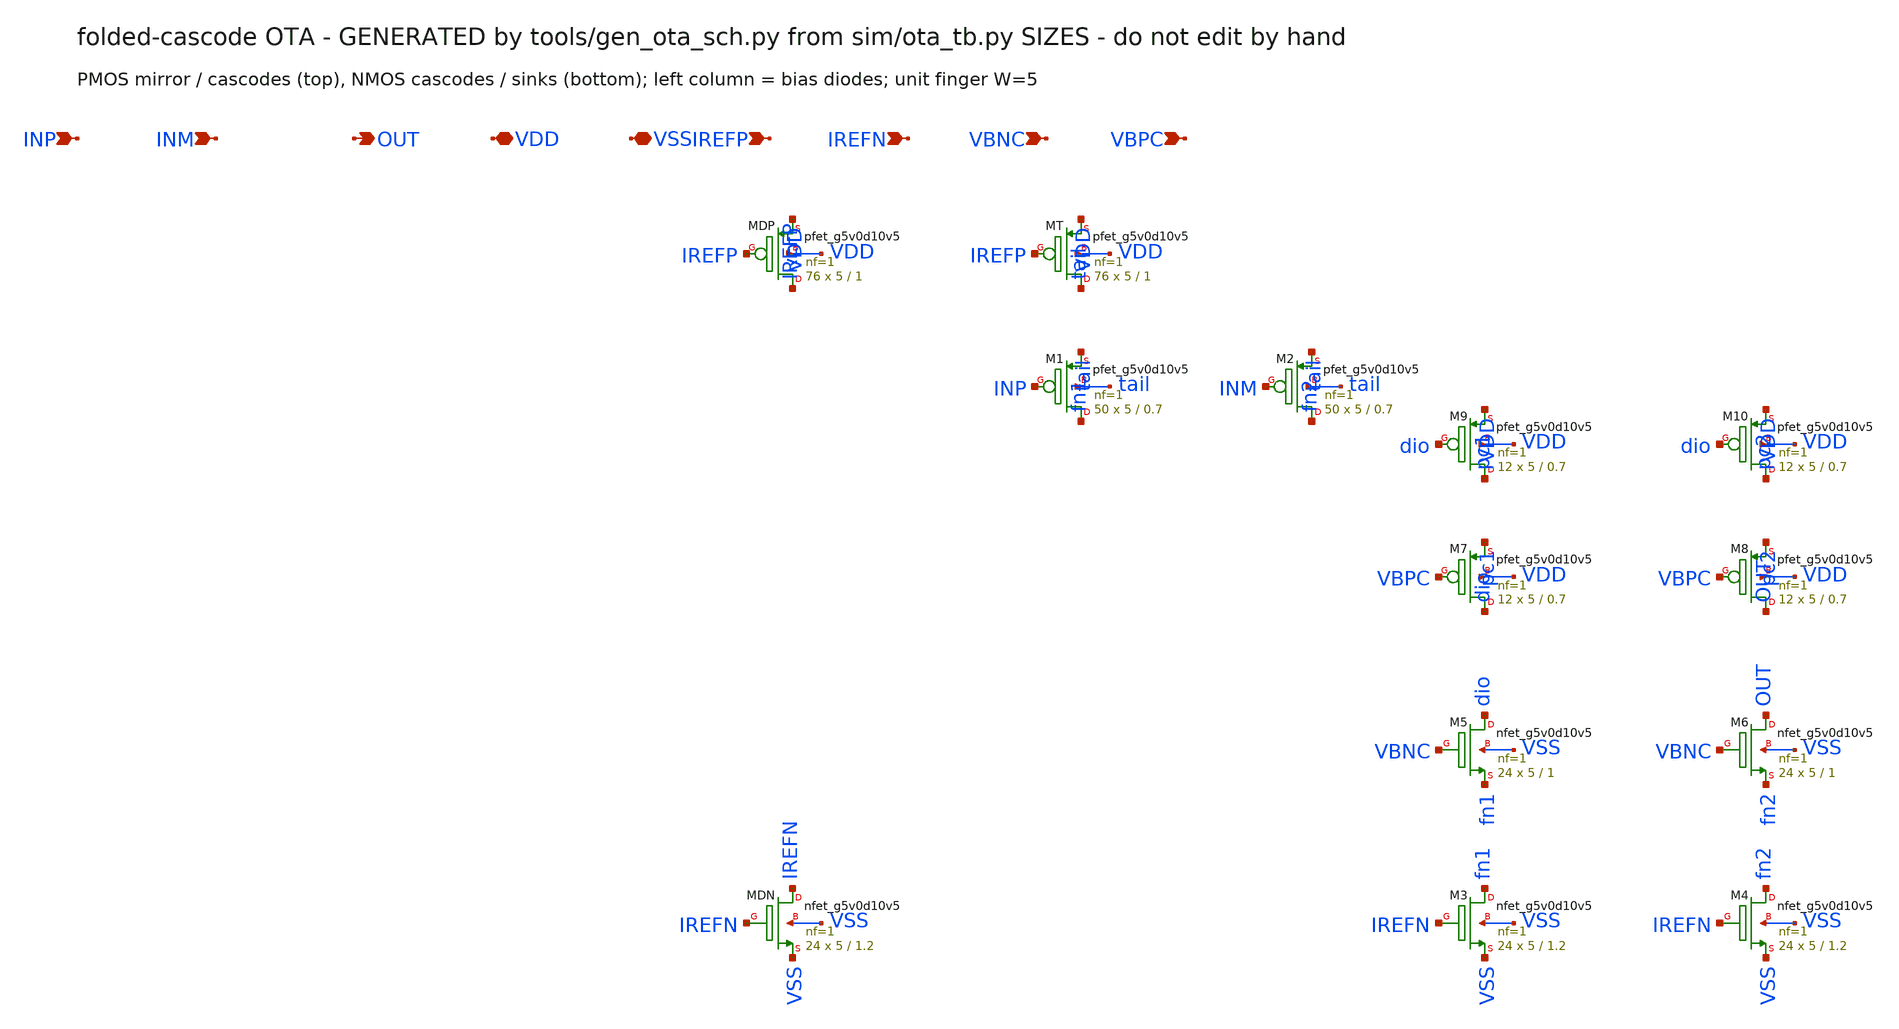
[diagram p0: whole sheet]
** sch_path: xschem/ota.sch
**.subckt ota INP INM OUT VDD VSS IREFP IREFN VBNC VBPC
*.ipin INP
*.ipin INM
*.opin OUT
*.iopin VDD
*.iopin VSS
*.ipin IREFP
*.ipin IREFN
*.ipin VBNC
*.ipin VBPC
XMDP IREFP IREFP VDD VDD sky130_fd_pr__pfet_g5v0d10v5 L=1 W=5 nf=1 ad=0 as=0 pd=0 ps=0 nrd=0 nrs=0
+ sa=0 sb=0 sd=0 mult=76 m=76
XMT tail IREFP VDD VDD sky130_fd_pr__pfet_g5v0d10v5 L=1 W=5 nf=1 ad=0 as=0 pd=0 ps=0 nrd=0 nrs=0
+ sa=0 sb=0 sd=0 mult=76 m=76
XM1 fn1 INP tail tail sky130_fd_pr__pfet_g5v0d10v5 L=0.7 W=5 nf=1 ad=0 as=0 pd=0 ps=0 nrd=0 nrs=0
+ sa=0 sb=0 sd=0 mult=50 m=50
XM2 fn2 INM tail tail sky130_fd_pr__pfet_g5v0d10v5 L=0.7 W=5 nf=1 ad=0 as=0 pd=0 ps=0 nrd=0 nrs=0
+ sa=0 sb=0 sd=0 mult=50 m=50
XM9 pc1 dio VDD VDD sky130_fd_pr__pfet_g5v0d10v5 L=0.7 W=5 nf=1 ad=0 as=0 pd=0 ps=0 nrd=0 nrs=0 sa=0
+ sb=0 sd=0 mult=12 m=12
XM10 pc2 dio VDD VDD sky130_fd_pr__pfet_g5v0d10v5 L=0.7 W=5 nf=1 ad=0 as=0 pd=0 ps=0 nrd=0 nrs=0
+ sa=0 sb=0 sd=0 mult=12 m=12
XM7 dio VBPC pc1 VDD sky130_fd_pr__pfet_g5v0d10v5 L=0.7 W=5 nf=1 ad=0 as=0 pd=0 ps=0 nrd=0 nrs=0
+ sa=0 sb=0 sd=0 mult=12 m=12
XM8 OUT VBPC pc2 VDD sky130_fd_pr__pfet_g5v0d10v5 L=0.7 W=5 nf=1 ad=0 as=0 pd=0 ps=0 nrd=0 nrs=0
+ sa=0 sb=0 sd=0 mult=12 m=12
XM5 dio VBNC fn1 VSS sky130_fd_pr__nfet_g5v0d10v5 L=1 W=5 nf=1 ad=0 as=0 pd=0 ps=0 nrd=0 nrs=0 sa=0
+ sb=0 sd=0 mult=24 m=24
XM6 OUT VBNC fn2 VSS sky130_fd_pr__nfet_g5v0d10v5 L=1 W=5 nf=1 ad=0 as=0 pd=0 ps=0 nrd=0 nrs=0 sa=0
+ sb=0 sd=0 mult=24 m=24
XM3 fn1 IREFN VSS VSS sky130_fd_pr__nfet_g5v0d10v5 L=1.2 W=5 nf=1 ad=0 as=0 pd=0 ps=0 nrd=0 nrs=0
+ sa=0 sb=0 sd=0 mult=24 m=24
XM4 fn2 IREFN VSS VSS sky130_fd_pr__nfet_g5v0d10v5 L=1.2 W=5 nf=1 ad=0 as=0 pd=0 ps=0 nrd=0 nrs=0
+ sa=0 sb=0 sd=0 mult=24 m=24
XMDN IREFN IREFN VSS VSS sky130_fd_pr__nfet_g5v0d10v5 L=1.2 W=5 nf=1 ad=0 as=0 pd=0 ps=0 nrd=0 nrs=0
+ sa=0 sb=0 sd=0 mult=24 m=24
**.ends
.end
